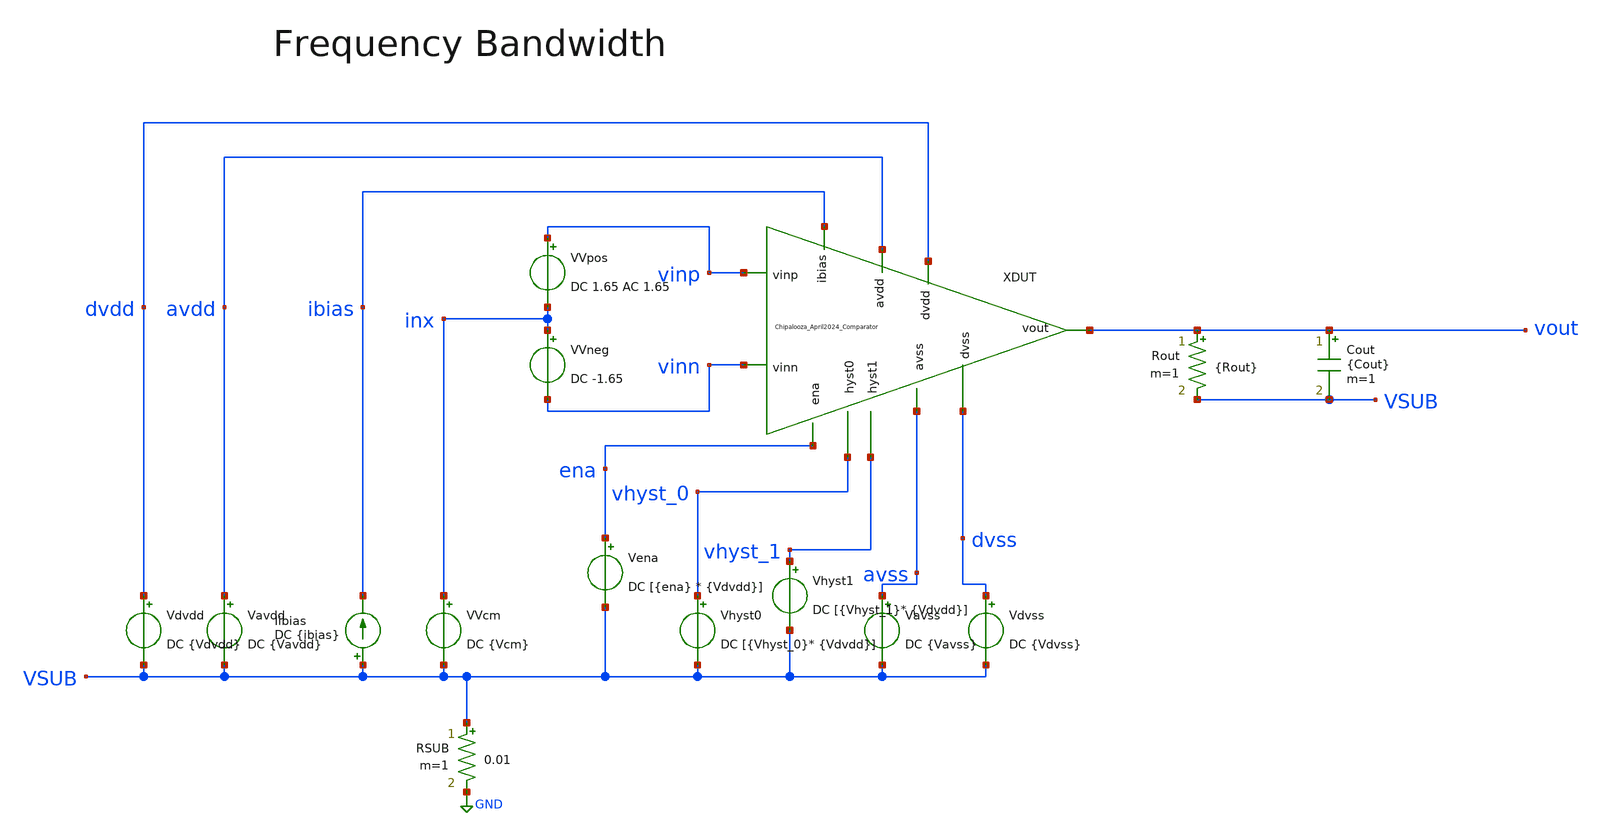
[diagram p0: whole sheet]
** sch_path: Chipalooza_April2024_Comparator/cace/frequencyBandwidth.sch
**.subckt frequencyBandwidth
Vavdd avdd VSUB DC {Vavdd}
Rout vout VSUB {Rout} m=1
Cout vout VSUB {Cout} m=1
Vdvdd dvdd VSUB DC {Vdvdd}
Vena ena VSUB DC [{ena} * {Vdvdd}]
Vhyst0 vhyst_0 VSUB DC [{Vhyst_0}* {Vdvdd}]
Vhyst1 vhyst_1 VSUB DC [{Vhyst_1}* {Vdvdd}]
Vavss avss VSUB DC {Vavss}
Vdvss dvss VSUB DC {Vdvss}
RSUB VSUB GND 0.01 m=1
Iibias VSUB ibias DC {ibias}
XDUT vhyst_0 vhyst_1 avdd vinp avss vinn dvdd dvss vout ibias ena Chipalooza_April2024_Comparator
VVpos vinp inx DC 1.65 AC 1.65
VVneg inx vinn DC -1.65
VVcm inx VSUB DC {Vcm}
**** begin user architecture code

.control

ac dec 20 1 1e12
plot v(vout)
plot v(dvdd)
plot v(avdd)

meas ac peak MAX vmag(vout) FROM=2 TO=1.5GHz
let f3db = peak/sqrt(2)
meas ac f1 when vmag(vout)=f3db RISE=1
meas ac f2 when vmag(vout)=f3db FALL=1

let f3 = $&f2
echo $&f3 > {simpath}/{filename}_{N}.data

write ngspice/frequencyBandwidth.raw

.endc



* CACE gensim simulation file {filename}_{N}
* Generated by CACE gensim, Efabless Corporation (c) 2023
* Find the current through the amplifier under condition of static input

.include {DUT_path}

.lib {PDK_ROOT}/{PDK}/libs.tech/combined/sky130.lib.spice {corner}

.option TEMP={temperature}
* Flag unsafe operating conditions (exceeds models' specified limits)
.option warn=1
.option savecurrents
.option save all


**** end user architecture code
**.ends
.GLOBAL GND
.end
